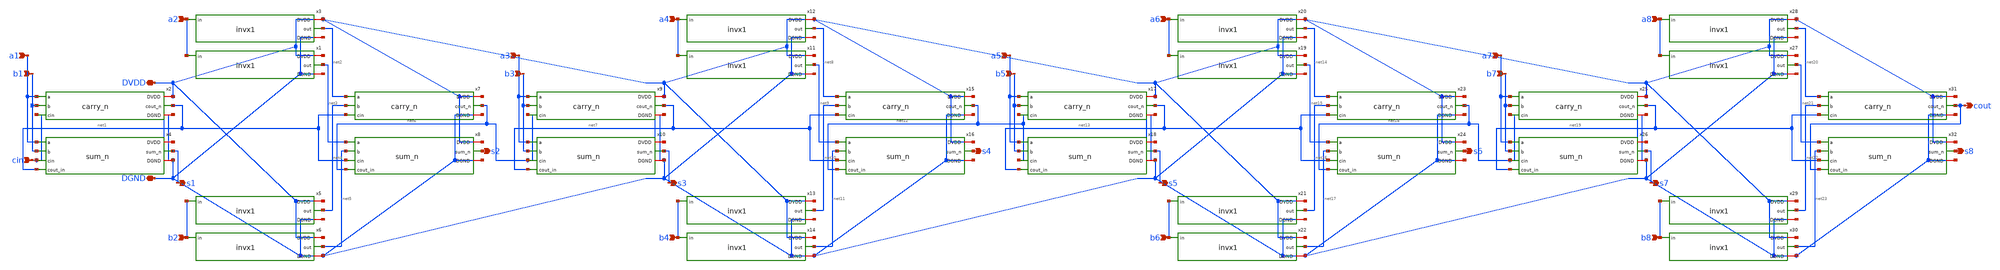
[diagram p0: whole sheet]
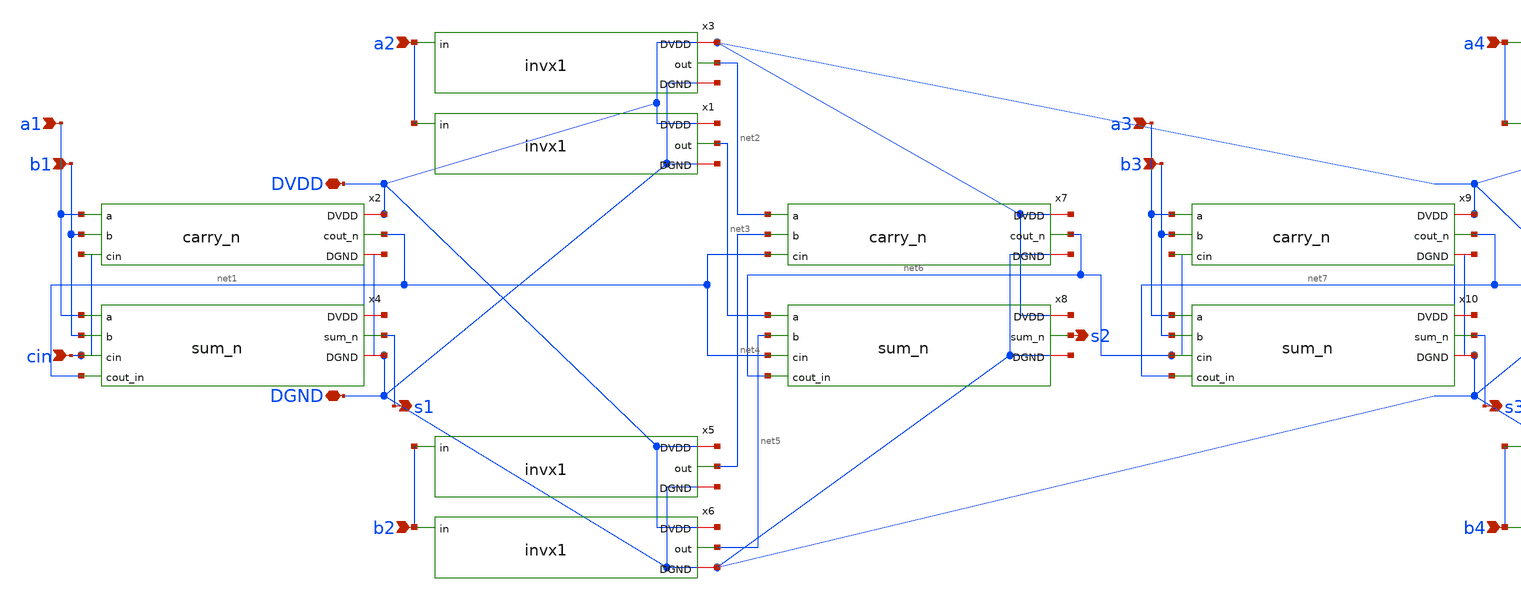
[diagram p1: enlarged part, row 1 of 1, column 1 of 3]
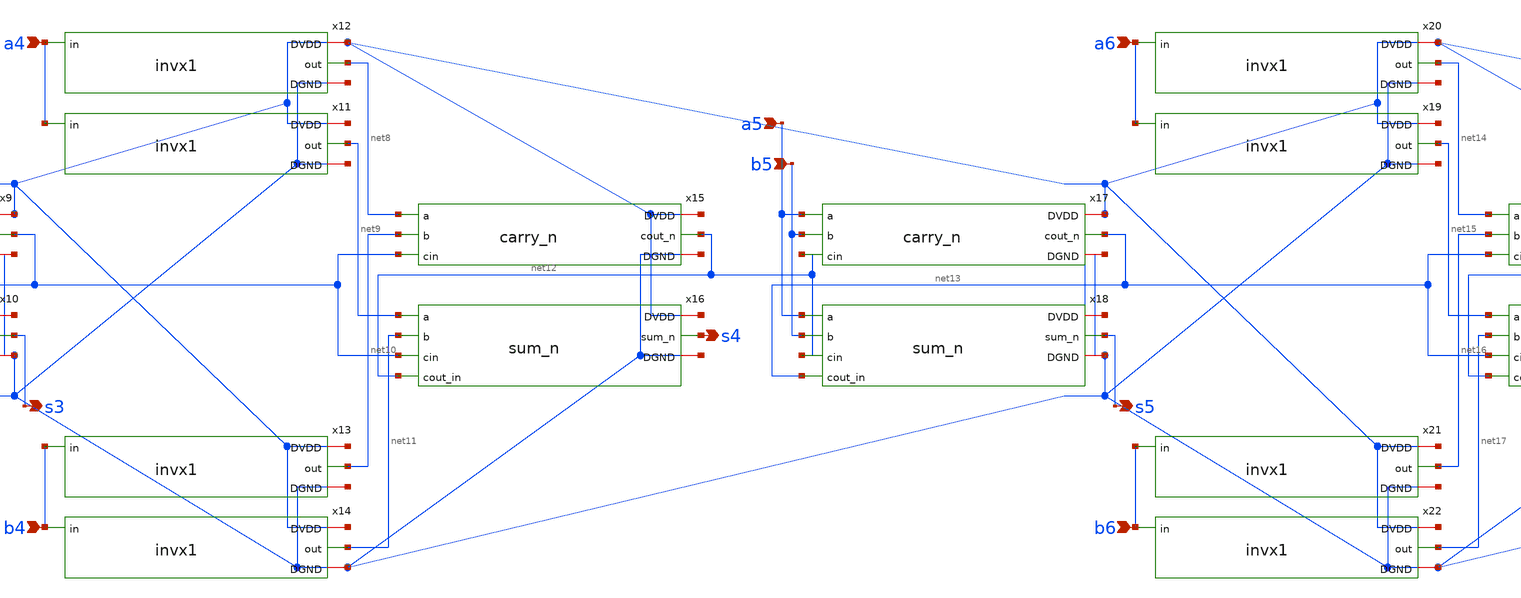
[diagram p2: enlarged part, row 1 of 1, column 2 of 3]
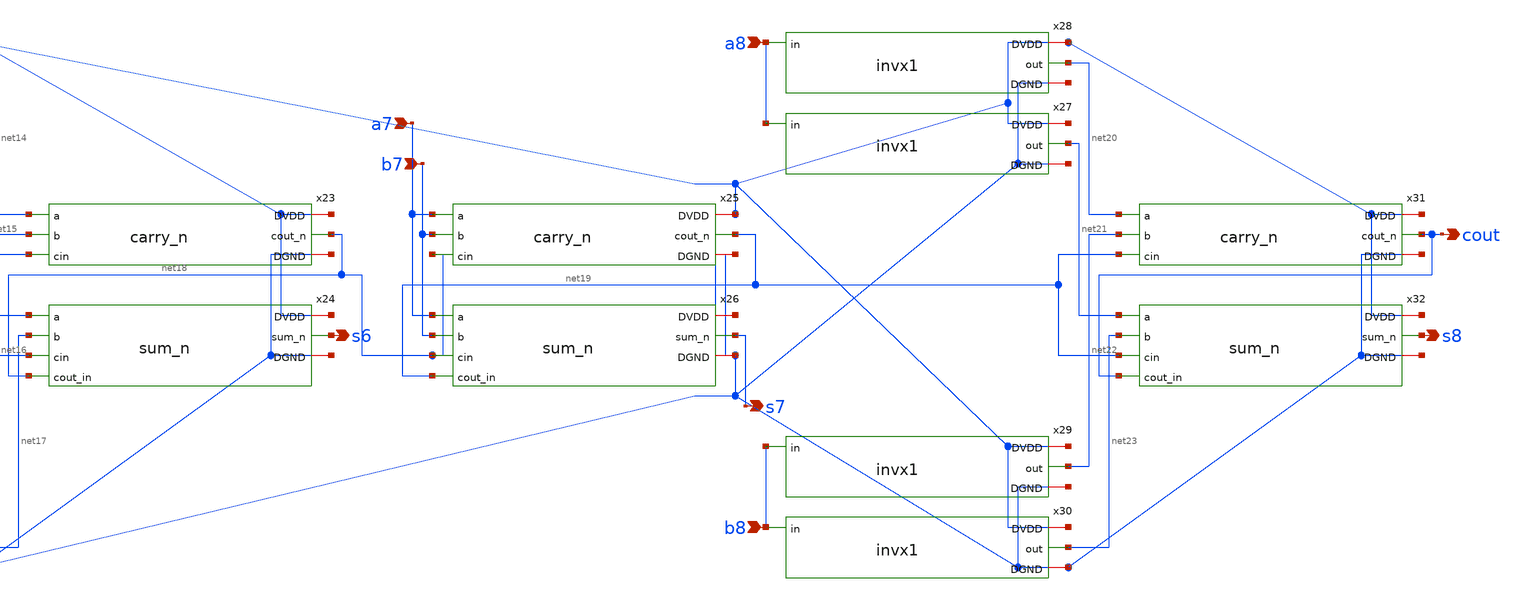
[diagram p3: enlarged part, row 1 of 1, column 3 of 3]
** sch_path: tut6/rca/incr/rca8b.sch
**.subckt rca8b cin a1 b1 DVDD DGND s1 a2 b2 s2 a3 b3 s3 a4 b4 s4 a5 b5 s5 a6 b6 s6 a7 b7 s7 cout a8
*+ b8 s8
*.ipin cin
*.ipin a1
*.ipin b1
*.iopin DVDD
*.iopin DGND
*.opin s1
*.ipin a2
*.ipin b2
*.opin s2
*.ipin a3
*.ipin b3
*.opin s3
*.ipin a4
*.ipin b4
*.opin s4
*.ipin a5
*.ipin b5
*.opin s5
*.ipin a6
*.ipin b6
*.opin s6
*.ipin a7
*.ipin b7
*.opin s7
*.opin cout
*.ipin a8
*.ipin b8
*.opin s8
x2 DVDD a1 b1 net1 cin DGND carry_n
x4 DVDD a1 b1 s1 cin net1 DGND sum_n
x1 DVDD a2 net3 DGND invx1
x3 DVDD a2 net2 DGND invx1
x5 DVDD b2 net4 DGND invx1
x6 DVDD b2 net5 DGND invx1
x7 DVDD net2 net4 net6 net1 DGND carry_n
x8 DVDD net3 net5 s2 net1 net6 DGND sum_n
x9 DVDD a3 b3 net7 net6 DGND carry_n
x10 DVDD a3 b3 s3 net6 net7 DGND sum_n
x11 DVDD a4 net9 DGND invx1
x12 DVDD a4 net8 DGND invx1
x13 DVDD b4 net10 DGND invx1
x14 DVDD b4 net11 DGND invx1
x15 DVDD net8 net10 net12 net7 DGND carry_n
x16 DVDD net9 net11 s4 net7 net12 DGND sum_n
x17 DVDD a5 b5 net13 net12 DGND carry_n
x18 DVDD a5 b5 s5 net12 net13 DGND sum_n
x19 DVDD a6 net15 DGND invx1
x20 DVDD a6 net14 DGND invx1
x21 DVDD b6 net16 DGND invx1
x22 DVDD b6 net17 DGND invx1
x23 DVDD net14 net16 net18 net13 DGND carry_n
x24 DVDD net15 net17 s6 net13 net18 DGND sum_n
x25 DVDD a7 b7 net19 net18 DGND carry_n
x26 DVDD a7 b7 s7 net18 net19 DGND sum_n
x27 DVDD a8 net21 DGND invx1
x28 DVDD a8 net20 DGND invx1
x29 DVDD b8 net22 DGND invx1
x30 DVDD b8 net23 DGND invx1
x31 DVDD net20 net22 cout net19 DGND carry_n
x32 DVDD net21 net23 s8 net19 cout DGND sum_n
**.ends
.end
